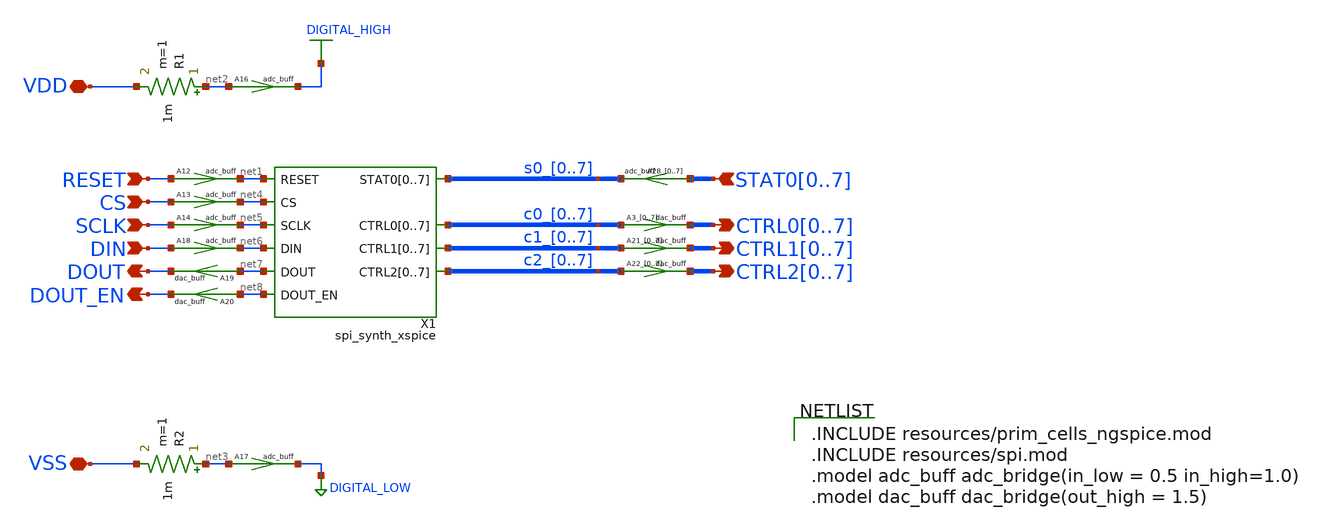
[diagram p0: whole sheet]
** sch_path: ip/spi/xschem/spi_xspice.sch
**.subckt spi_xspice VSS VDD RESET DOUT CS SCLK DIN DOUT_EN
*+ CTRL00,CTRL01,CTRL02,CTRL03,CTRL04,CTRL05,CTRL06,CTRL07 CTRL10,CTRL11,CTRL12,CTRL13,CTRL14,CTRL15,CTRL16,CTRL17
*+ CTRL20,CTRL21,CTRL22,CTRL23,CTRL24,CTRL25,CTRL26,CTRL27 STAT00,STAT01,STAT02,STAT03,STAT04,STAT05,STAT06,STAT07
*.iopin VSS
*.iopin VDD
*.ipin RESET
*.opin DOUT
*.ipin CS
*.ipin SCLK
*.ipin DIN
*.opin DOUT_EN
*.opin CTRL00,CTRL01,CTRL02,CTRL03,CTRL04,CTRL05,CTRL06,CTRL07
*.opin CTRL10,CTRL11,CTRL12,CTRL13,CTRL14,CTRL15,CTRL16,CTRL17
*.opin CTRL20,CTRL21,CTRL22,CTRL23,CTRL24,CTRL25,CTRL26,CTRL27
*.ipin STAT00,STAT01,STAT02,STAT03,STAT04,STAT05,STAT06,STAT07
A3_0 [ c0_0 ] [ CTRL00 ] dac_buff
A3_1 [ c0_1 ] [ CTRL01 ] dac_buff
A3_2 [ c0_2 ] [ CTRL02 ] dac_buff
A3_3 [ c0_3 ] [ CTRL03 ] dac_buff
A3_4 [ c0_4 ] [ CTRL04 ] dac_buff
A3_5 [ c0_5 ] [ CTRL05 ] dac_buff
A3_6 [ c0_6 ] [ CTRL06 ] dac_buff
A3_7 [ c0_7 ] [ CTRL07 ] dac_buff
A12 [ RESET ] [ net1 ] adc_buff
R1 net2 VDD 1m m=1
R2 net3 VSS 1m m=1
A16 [ net2 ] [ DIGITAL_HIGH ] adc_buff
A17 [ net3 ] [ DIGITAL_LOW ] adc_buff
A13 [ CS ] [ net4 ] adc_buff
A14 [ SCLK ] [ net5 ] adc_buff
A18 [ DIN ] [ net6 ] adc_buff
A19 [ net7 ] [ DOUT ] dac_buff
A20 [ net8 ] [ DOUT_EN ] dac_buff
A21_0 [ c1_0 ] [ CTRL10 ] dac_buff
A21_1 [ c1_1 ] [ CTRL11 ] dac_buff
A21_2 [ c1_2 ] [ CTRL12 ] dac_buff
A21_3 [ c1_3 ] [ CTRL13 ] dac_buff
A21_4 [ c1_4 ] [ CTRL14 ] dac_buff
A21_5 [ c1_5 ] [ CTRL15 ] dac_buff
A21_6 [ c1_6 ] [ CTRL16 ] dac_buff
A21_7 [ c1_7 ] [ CTRL17 ] dac_buff
A22_0 [ c2_0 ] [ CTRL20 ] dac_buff
A22_1 [ c2_1 ] [ CTRL21 ] dac_buff
A22_2 [ c2_2 ] [ CTRL22 ] dac_buff
A22_3 [ c2_3 ] [ CTRL23 ] dac_buff
A22_4 [ c2_4 ] [ CTRL24 ] dac_buff
A22_5 [ c2_5 ] [ CTRL25 ] dac_buff
A22_6 [ c2_6 ] [ CTRL26 ] dac_buff
A22_7 [ c2_7 ] [ CTRL27 ] dac_buff
A28_0 [ STAT00 ] [ s0_0 ] adc_buff
A28_1 [ STAT01 ] [ s0_1 ] adc_buff
A28_2 [ STAT02 ] [ s0_2 ] adc_buff
A28_3 [ STAT03 ] [ s0_3 ] adc_buff
A28_4 [ STAT04 ] [ s0_4 ] adc_buff
A28_5 [ STAT05 ] [ s0_5 ] adc_buff
A28_6 [ STAT06 ] [ s0_6 ] adc_buff
A28_7 [ STAT07 ] [ s0_7 ] adc_buff
X1 net1 net4 net5 net6 net7 net8 c0_0 c0_1 c0_2 c0_3 c0_4 c0_5 c0_6 c0_7 c1_0 c1_1 c1_2 c1_3 c1_4
+ c1_5 c1_6 c1_7 c2_0 c2_1 c2_2 c2_3 c2_4 c2_5 c2_6 c2_7 s0_0 s0_1 s0_2 s0_3 s0_4 s0_5 s0_6 s0_7 spi
**** begin user architecture code

.INCLUDE resources/prim_cells_ngspice.mod
.INCLUDE resources/spi.mod
.model adc_buff adc_bridge(in_low = 0.5 in_high=1.0)
.model dac_buff dac_bridge(out_high = 1.5)

**** end user architecture code
**.ends
.GLOBAL DIGITAL_HIGH
.GLOBAL DIGITAL_LOW
.end
